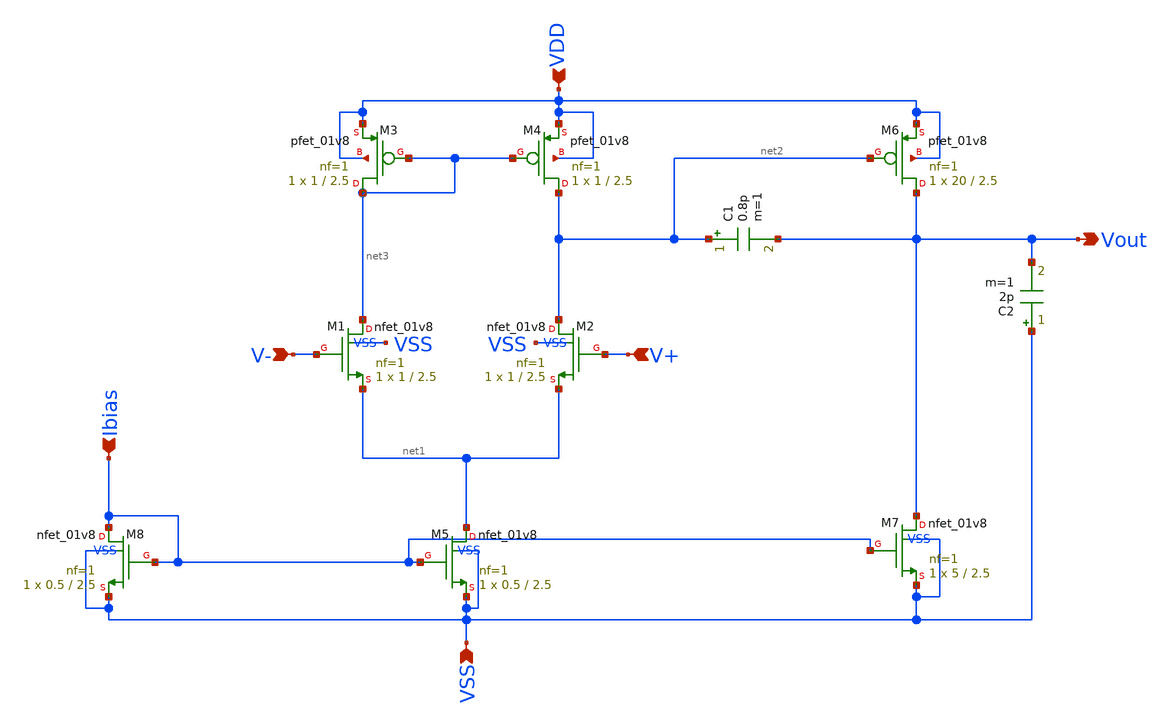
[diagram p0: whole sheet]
** sch_path: ttsky25a-opamp/xschem/2stageCMOSOpAmp.sch
**.subckt 2stageCMOSOpAmp VDD VSS Vout V+ V- Ibias
*.ipin VDD
*.ipin VSS
*.opin Vout
*.ipin V+
*.ipin V-
*.ipin Ibias
C1 net2 Vout 0.8p m=1
C2 VSS Vout 2p m=1
XM1 net3 V- net1 VSS sky130_fd_pr__nfet_01v8 L=2.5 W=1 nf=1 ad='int((nf+1)/2) * W/nf * 0.29' as='int((nf+2)/2) * W/nf * 0.29'
+ pd='2*int((nf+1)/2) * (W/nf + 0.29)' ps='2*int((nf+2)/2) * (W/nf + 0.29)' nrd='0.29 / W' nrs='0.29 / W'
+ sa=0 sb=0 sd=0 mult=1 m=1
XM2 net2 V+ net1 VSS sky130_fd_pr__nfet_01v8 L=2.5 W=1 nf=1 ad='int((nf+1)/2) * W/nf * 0.29' as='int((nf+2)/2) * W/nf * 0.29'
+ pd='2*int((nf+1)/2) * (W/nf + 0.29)' ps='2*int((nf+2)/2) * (W/nf + 0.29)' nrd='0.29 / W' nrs='0.29 / W'
+ sa=0 sb=0 sd=0 mult=1 m=1
XM3 net3 net3 VDD VDD sky130_fd_pr__pfet_01v8 L=2.5 W=1 nf=1 ad='int((nf+1)/2) * W/nf * 0.29' as='int((nf+2)/2) * W/nf * 0.29'
+ pd='2*int((nf+1)/2) * (W/nf + 0.29)' ps='2*int((nf+2)/2) * (W/nf + 0.29)' nrd='0.29 / W' nrs='0.29 / W'
+ sa=0 sb=0 sd=0 mult=1 m=1
XM4 net2 net3 VDD VDD sky130_fd_pr__pfet_01v8 L=2.5 W=1 nf=1 ad='int((nf+1)/2) * W/nf * 0.29' as='int((nf+2)/2) * W/nf * 0.29'
+ pd='2*int((nf+1)/2) * (W/nf + 0.29)' ps='2*int((nf+2)/2) * (W/nf + 0.29)' nrd='0.29 / W' nrs='0.29 / W'
+ sa=0 sb=0 sd=0 mult=1 m=1
XM6 Vout net2 VDD VDD sky130_fd_pr__pfet_01v8 L=2.5 W=20 nf=1 ad='int((nf+1)/2) * W/nf * 0.29' as='int((nf+2)/2) * W/nf * 0.29'
+ pd='2*int((nf+1)/2) * (W/nf + 0.29)' ps='2*int((nf+2)/2) * (W/nf + 0.29)' nrd='0.29 / W' nrs='0.29 / W'
+ sa=0 sb=0 sd=0 mult=1 m=1
XM5 net1 Ibias VSS VSS sky130_fd_pr__nfet_01v8 L=2.5 W=0.5 nf=1 ad='int((nf+1)/2) * W/nf * 0.29' as='int((nf+2)/2) * W/nf * 0.29'
+ pd='2*int((nf+1)/2) * (W/nf + 0.29)' ps='2*int((nf+2)/2) * (W/nf + 0.29)' nrd='0.29 / W' nrs='0.29 / W'
+ sa=0 sb=0 sd=0 mult=1 m=1
XM8 Ibias Ibias VSS VSS sky130_fd_pr__nfet_01v8 L=2.5 W=0.5 nf=1 ad='int((nf+1)/2) * W/nf * 0.29' as='int((nf+2)/2) * W/nf * 0.29'
+ pd='2*int((nf+1)/2) * (W/nf + 0.29)' ps='2*int((nf+2)/2) * (W/nf + 0.29)' nrd='0.29 / W' nrs='0.29 / W'
+ sa=0 sb=0 sd=0 mult=1 m=1
XM7 Vout Ibias VSS VSS sky130_fd_pr__nfet_01v8 L=2.5 W=5 nf=1 ad='int((nf+1)/2) * W/nf * 0.29' as='int((nf+2)/2) * W/nf * 0.29'
+ pd='2*int((nf+1)/2) * (W/nf + 0.29)' ps='2*int((nf+2)/2) * (W/nf + 0.29)' nrd='0.29 / W' nrs='0.29 / W'
+ sa=0 sb=0 sd=0 mult=1 m=1
**.ends
.end
